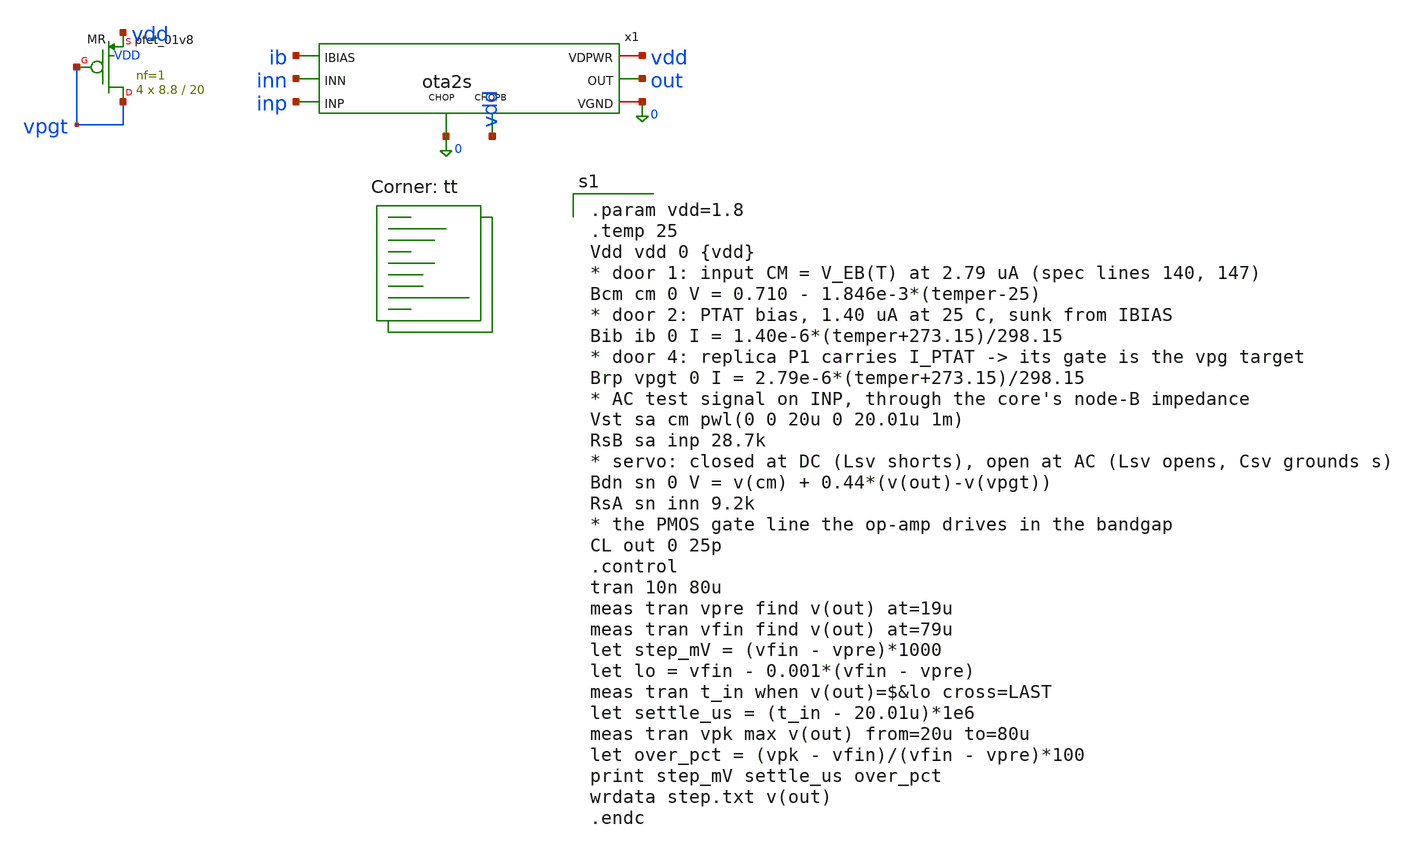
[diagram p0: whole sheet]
** sch_path: xschem/tb_ota2s_tran.sch
**.subckt tb_ota2s_tran
x1 inp inn out vdd 0 ib 0 vdd ota2s
XMR vpgt vpgt vdd VDD sky130_fd_pr__pfet_01v8 L=20 W=8.8 nf=1 ad='int((1 + 1)/2) * 8.8 / 1 * 0.29' as='int((1 + 2)/2) * 8.8 / 1 * 0.29'
+ pd='2*int((1 + 1)/2) * (8.8 / 1 + 0.29)' ps='2*int((1 + 2)/2) * (8.8 / 1 + 0.29)' nrd='0.29 / 8.8 ' nrs='0.29 / 8.8 '
+ sa=0 sb=0 sd=0 mult=4 m=4
**** begin user architecture code
.lib $::SKYWATER_MODELS/sky130.lib.spice tt

.param vdd=1.8
.temp 25
Vdd vdd 0 {vdd}
* door 1: input CM = V_EB(T) at 2.79 uA (spec lines 140, 147)
Bcm cm 0 V = 0.710 - 1.846e-3*(temper-25)
* door 2: PTAT bias, 1.40 uA at 25 C, sunk from IBIAS
Bib ib 0 I = 1.40e-6*(temper+273.15)/298.15
* door 4: replica P1 carries I_PTAT -> its gate is the vpg target
Brp vpgt 0 I = 2.79e-6*(temper+273.15)/298.15
* AC test signal on INP, through the core's node-B impedance
Vst sa cm pwl(0 0 20u 0 20.01u 1m)
RsB sa inp 28.7k
* servo: closed at DC (Lsv shorts), open at AC (Lsv opens, Csv grounds s)
Bdn sn 0 V = v(cm) + 0.44*(v(out)-v(vpgt))
RsA sn inn 9.2k
* the PMOS gate line the op-amp drives in the bandgap
CL out 0 25p
.control
tran 10n 80u
meas tran vpre find v(out) at=19u
meas tran vfin find v(out) at=79u
let step_mV = (vfin - vpre)*1000
let lo = vfin - 0.001*(vfin - vpre)
meas tran t_in when v(out)=$&lo cross=LAST
let settle_us = (t_in - 20.01u)*1e6
meas tran vpk max v(out) from=20u to=80u
let over_pct = (vpk - vfin)/(vfin - vpre)*100
print step_mV settle_us over_pct
wrdata step.txt v(out)
.endc

**** end user architecture code
**.ends

* expanding   symbol:  ota2s.sym # of pins=8
** sym_path: xschem/ota2s.sym
** sch_path: xschem/ota2s.sch
.subckt ota2s INP INN OUT VDPWR VGND IBIAS CHOP CHOPB
*.ipin INN
*.ipin INP
*.ipin IBIAS
*.opin OUT
*.iopin VDPWR
*.iopin VGND
*.ipin CHOPB
*.ipin CHOP
XMREF IBIAS IBIAS VDPWR VDPWR sky130_fd_pr__pfet_01v8 L=4 W=20 nf=1 ad='int((1 + 1)/2) * 20 / 1 * 0.29' as='int((1
+ + 2)/2) * 20 / 1 * 0.29' pd='2*int((1 + 1)/2) * (20 / 1 + 0.29)' ps='2*int((1 + 2)/2) * (20 / 1 + 0.29)' nrd='0.29
+ / 20 ' nrs='0.29 / 20 ' sa=0 sb=0 sd=0 mult=1 m=1
XMTAIL tail IBIAS VDPWR VDPWR sky130_fd_pr__pfet_01v8 L=4 W=20 nf=1 ad='int((1 + 1)/2) * 20 / 1 * 0.29' as='int((1
+ + 2)/2) * 20 / 1 * 0.29' pd='2*int((1 + 1)/2) * (20 / 1 + 0.29)' ps='2*int((1 + 2)/2) * (20 / 1 + 0.29)' nrd='0.29
+ / 20 ' nrs='0.29 / 20 ' sa=0 sb=0 sd=0 mult=2 m=2
XMP1 d1 INN tail VDPWR sky130_fd_pr__pfet_01v8_lvt L=6 W=25 nf=1 ad='int((1 + 1)/2) * 25 / 1 * 0.29' as='int((1
+ + 2)/2) * 25 / 1 * 0.29' pd='2*int((1 + 1)/2) * (25 / 1 + 0.29)' ps='2*int((1 + 2)/2) * (25 / 1 + 0.29)' nrd='0.29
+ / 25 ' nrs='0.29 / 25 ' sa=0 sb=0 sd=0 mult=24 m=24
XMP2 x1 INP tail VDPWR sky130_fd_pr__pfet_01v8_lvt L=6 W=25 nf=1 ad='int((1 + 1)/2) * 25 / 1 * 0.29' as='int((1
+ + 2)/2) * 25 / 1 * 0.29' pd='2*int((1 + 1)/2) * (25 / 1 + 0.29)' ps='2*int((1 + 2)/2) * (25 / 1 + 0.29)' nrd='0.29
+ / 25 ' nrs='0.29 / 25 ' sa=0 sb=0 sd=0 mult=24 m=24
XMN1 d1 g12 VGND VGND sky130_fd_pr__nfet_01v8 L=20 W=6 nf=1 ad='int((1 + 1)/2) * 6 / 1 * 0.29' as='int((1
+ + 2)/2) * 6 / 1 * 0.29' pd='2*int((1 + 1)/2) * (6 / 1 + 0.29)' ps='2*int((1 + 2)/2) * (6 / 1 + 0.29)' nrd='0.29
+ / 6 ' nrs='0.29 / 6 ' sa=0 sb=0 sd=0 mult=2 m=2
XMN2 x1 g12 VGND VGND sky130_fd_pr__nfet_01v8 L=20 W=6 nf=1 ad='int((1 + 1)/2) * 6 / 1 * 0.29' as='int((1
+ + 2)/2) * 6 / 1 * 0.29' pd='2*int((1 + 1)/2) * (6 / 1 + 0.29)' ps='2*int((1 + 2)/2) * (6 / 1 + 0.29)' nrd='0.29
+ / 6 ' nrs='0.29 / 6 ' sa=0 sb=0 sd=0 mult=2 m=2
XMP3 OUT IBIAS VDPWR VDPWR sky130_fd_pr__pfet_01v8 L=4 W=20 nf=1 ad='int((1 + 1)/2) * 20 / 1 * 0.29' as='int((1
+ + 2)/2) * 20 / 1 * 0.29' pd='2*int((1 + 1)/2) * (20 / 1 + 0.29)' ps='2*int((1 + 2)/2) * (20 / 1 + 0.29)' nrd='0.29
+ / 20 ' nrs='0.29 / 20 ' sa=0 sb=0 sd=0 mult=6 m=6
XMN3 OUT g3 VGND VGND sky130_fd_pr__nfet_01v8 L=1 W=7 nf=1 ad='int((1 + 1)/2) * 7 / 1 * 0.29' as='int((1
+ + 2)/2) * 7 / 1 * 0.29' pd='2*int((1 + 1)/2) * (7 / 1 + 0.29)' ps='2*int((1 + 2)/2) * (7 / 1 + 0.29)' nrd='0.29
+ / 7 ' nrs='0.29 / 7 ' sa=0 sb=0 sd=0 mult=1 m=1
XRZ1 net1 g3 VGND sky130_fd_pr__res_high_po_1p41 L=20 mult=1 m=1
XRZ2 net2 net1 VGND sky130_fd_pr__res_high_po_1p41 L=20 mult=1 m=1
XRZ3 net3 net2 VGND sky130_fd_pr__res_high_po_1p41 L=20 mult=1 m=1
XRZ4 net4 net3 VGND sky130_fd_pr__res_high_po_1p41 L=20 mult=1 m=1
XRZ5 net5 net4 VGND sky130_fd_pr__res_high_po_1p41 L=20 mult=1 m=1
XRZ6 cz net5 VGND sky130_fd_pr__res_high_po_1p41 L=20 mult=1 m=1
XCC cz OUT sky130_fd_pr__cap_mim_m3_1 W=25 L=25 MF=8 m=8
XDP tail VDPWR tail VDPWR sky130_fd_pr__pfet_01v8_lvt L=6 W=25 nf=1 ad='int((1 + 1)/2) * 25 / 1 * 0.29' as='int((1
+ + 2)/2) * 25 / 1 * 0.29' pd='2*int((1 + 1)/2) * (25 / 1 + 0.29)' ps='2*int((1 + 2)/2) * (25 / 1 + 0.29)' nrd='0.29
+ / 25 ' nrs='0.29 / 25 ' sa=0 sb=0 sd=0 mult=8 m=8
XDNA d1 VGND VGND VGND sky130_fd_pr__nfet_01v8 L=20 W=6 nf=1 ad='int((1 + 1)/2) * 6 / 1 * 0.29' as='int((1
+ + 2)/2) * 6 / 1 * 0.29' pd='2*int((1 + 1)/2) * (6 / 1 + 0.29)' ps='2*int((1 + 2)/2) * (6 / 1 + 0.29)' nrd='0.29
+ / 6 ' nrs='0.29 / 6 ' sa=0 sb=0 sd=0 mult=2 m=2
XDNB x1 VGND VGND VGND sky130_fd_pr__nfet_01v8 L=20 W=6 nf=1 ad='int((1 + 1)/2) * 6 / 1 * 0.29' as='int((1
+ + 2)/2) * 6 / 1 * 0.29' pd='2*int((1 + 1)/2) * (6 / 1 + 0.29)' ps='2*int((1 + 2)/2) * (6 / 1 + 0.29)' nrd='0.29
+ / 6 ' nrs='0.29 / 6 ' sa=0 sb=0 sd=0 mult=2 m=2
XDB VDPWR VDPWR VDPWR VDPWR sky130_fd_pr__pfet_01v8 L=4 W=20 nf=1 ad='int((1 + 1)/2) * 20 / 1 * 0.29' as='int((1
+ + 2)/2) * 20 / 1 * 0.29' pd='2*int((1 + 1)/2) * (20 / 1 + 0.29)' ps='2*int((1 + 2)/2) * (20 / 1 + 0.29)' nrd='0.29
+ / 20 ' nrs='0.29 / 20 ' sa=0 sb=0 sd=0 mult=2 m=2
XRD1 VGND VGND VGND sky130_fd_pr__res_high_po_1p41 L=20 mult=1 m=1
XRD2 VGND VGND VGND sky130_fd_pr__res_high_po_1p41 L=20 mult=1 m=1
XSD1 d1 CHOPB g12 VGND sky130_fd_pr__nfet_01v8 L=0.5 W=6 nf=1 ad='int((1 + 1)/2) * 6 / 1 * 0.29' as='int((1
+ + 2)/2) * 6 / 1 * 0.29' pd='2*int((1 + 1)/2) * (6 / 1 + 0.29)' ps='2*int((1 + 2)/2) * (6 / 1 + 0.29)' nrd='0.29
+ / 6 ' nrs='0.29 / 6 ' sa=0 sb=0 sd=0 mult=1 m=1
XSD2 x1 CHOP g12 VGND sky130_fd_pr__nfet_01v8 L=0.5 W=6 nf=1 ad='int((1 + 1)/2) * 6 / 1 * 0.29' as='int((1
+ + 2)/2) * 6 / 1 * 0.29' pd='2*int((1 + 1)/2) * (6 / 1 + 0.29)' ps='2*int((1 + 2)/2) * (6 / 1 + 0.29)' nrd='0.29
+ / 6 ' nrs='0.29 / 6 ' sa=0 sb=0 sd=0 mult=1 m=1
XSG2 g3 CHOP d1 VGND sky130_fd_pr__nfet_01v8 L=0.5 W=6 nf=1 ad='int((1 + 1)/2) * 6 / 1 * 0.29' as='int((1
+ + 2)/2) * 6 / 1 * 0.29' pd='2*int((1 + 1)/2) * (6 / 1 + 0.29)' ps='2*int((1 + 2)/2) * (6 / 1 + 0.29)' nrd='0.29
+ / 6 ' nrs='0.29 / 6 ' sa=0 sb=0 sd=0 mult=1 m=1
XSG1 x1 CHOPB g3 VGND sky130_fd_pr__nfet_01v8 L=0.5 W=6 nf=1 ad='int((1 + 1)/2) * 6 / 1 * 0.29' as='int((1
+ + 2)/2) * 6 / 1 * 0.29' pd='2*int((1 + 1)/2) * (6 / 1 + 0.29)' ps='2*int((1 + 2)/2) * (6 / 1 + 0.29)' nrd='0.29
+ / 6 ' nrs='0.29 / 6 ' sa=0 sb=0 sd=0 mult=1 m=1
.ends

.end
